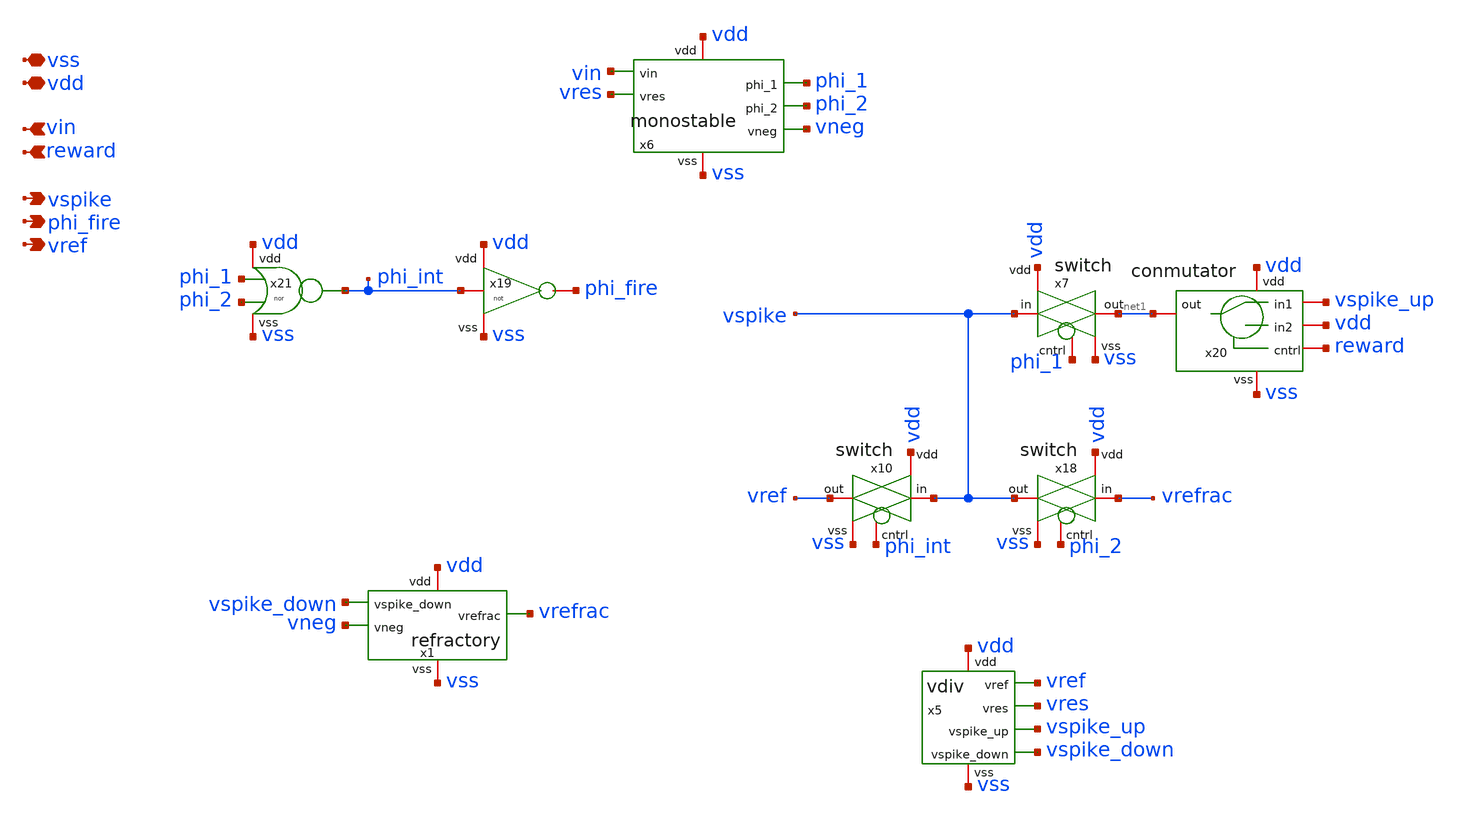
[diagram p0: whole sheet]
** sch_path: designs/libs/core_LIF_comp/core_phaseUpulse/phaseUpulse.sch
**.subckt phaseUpulse vin vdd vss vspike phi_fire vref reward
*.ipin vin
*.iopin vdd
*.iopin vss
*.opin vspike
*.opin phi_fire
*.opin vref
*.ipin reward
x19 vdd phi_int phi_fire vss not
x21 vdd vss phi_1 phi_2 phi_int nor
x7 vdd vspike net1 phi_1 vss switch
x10 vdd vspike vref phi_int vss switch
x18 vdd vrefrac vspike phi_2 vss switch
x20 reward vdd vdd net1 vspike_up vss conmutator
x5 vss vdd vref vspike_up vspike_down vres vdiv
x6 vss vdd vin vres phi_1 phi_2 vneg monostable
x1 vss vdd vspike_down vneg vrefrac refractory
**.ends
.end
